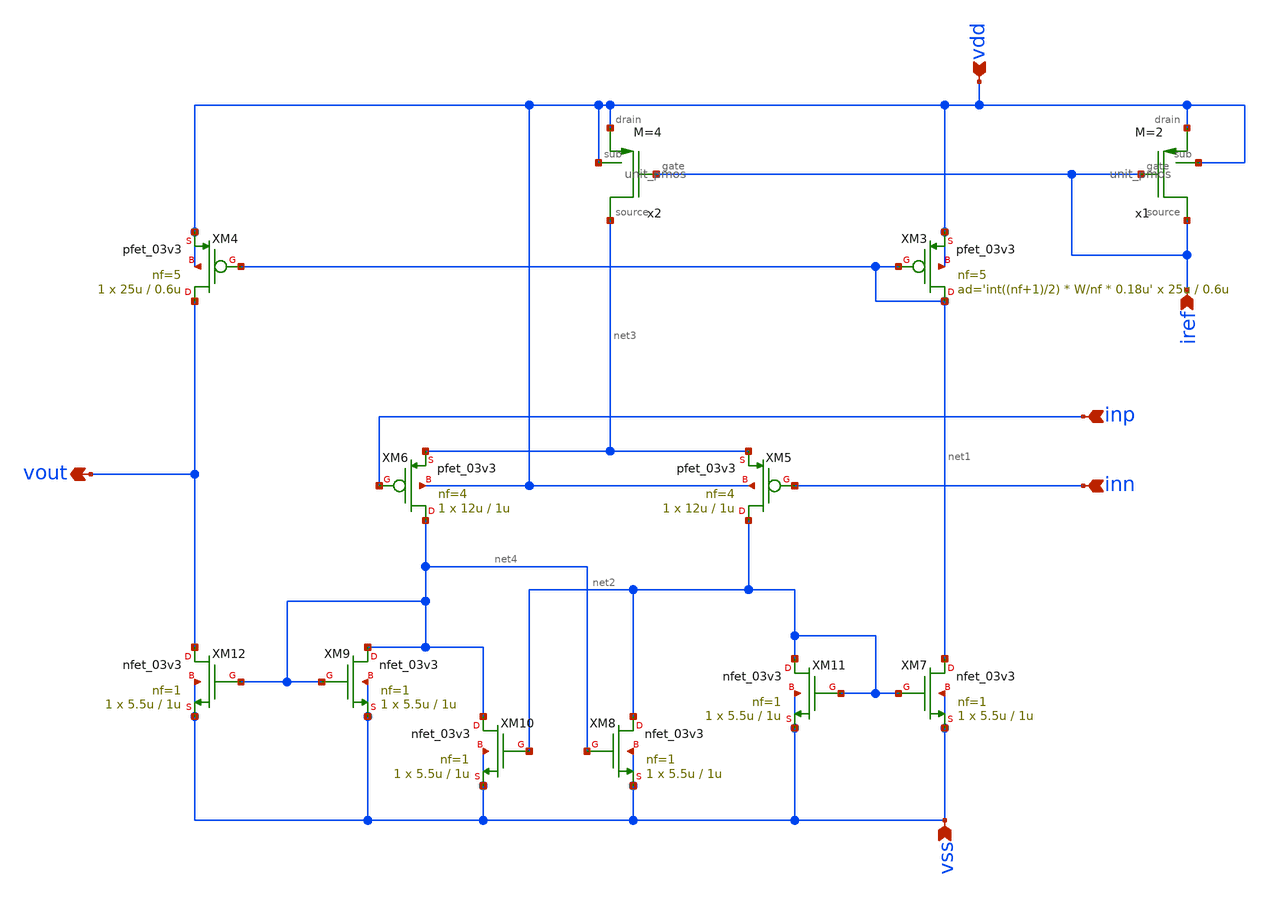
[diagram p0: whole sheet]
** sch_path: designs/libs/core_analog/Comparator/Pmos_Comparator.sch
**.subckt Pmos_Comparator vdd vss iref inn inp vout
*.ipin vdd
*.ipin vss
*.ipin iref
*.ipin inn
*.ipin inp
*.opin vout
XM3 net1 net1 vdd vdd pfet_03v3 L=0.6u W=25u nf=5 ad='int((nf+1)/2) * W/nf * 0.18u' as='int((nf+2)/2) * W/nf * 0.18u'
+ pd='2*int((nf+1)/2) * (W/nf + 0.18u)' ps='2*int((nf+2)/2) * (W/nf + 0.18u)' nrd='0.18u / W' nrs='0.18u / W'
+ sa=0 sb=0 sd=0 m=ad='int((nf+1)/2) * W/nf * 0.18u'
XM4 vout net1 vdd vdd pfet_03v3 L=0.6u W=25u nf=5 ad='int((nf+1)/2) * W/nf * 0.18u' as='int((nf+2)/2) * W/nf * 0.18u'
+ pd='2*int((nf+1)/2) * (W/nf + 0.18u)' ps='2*int((nf+2)/2) * (W/nf + 0.18u)' nrd='0.18u / W' nrs='0.18u / W'
+ sa=0 sb=0 sd=0 m=1
XM5 net2 inn net3 vdd pfet_03v3 L=1u W=12u nf=4 ad='int((nf+1)/2) * W/nf * 0.18u' as='int((nf+2)/2) * W/nf * 0.18u'
+ pd='2*int((nf+1)/2) * (W/nf + 0.18u)' ps='2*int((nf+2)/2) * (W/nf + 0.18u)' nrd='0.18u / W' nrs='0.18u / W'
+ sa=0 sb=0 sd=0 m=1
XM6 net4 inp net3 vdd pfet_03v3 L=1u W=12u nf=4 ad='int((nf+1)/2) * W/nf * 0.18u' as='int((nf+2)/2) * W/nf * 0.18u'
+ pd='2*int((nf+1)/2) * (W/nf + 0.18u)' ps='2*int((nf+2)/2) * (W/nf + 0.18u)' nrd='0.18u / W' nrs='0.18u / W'
+ sa=0 sb=0 sd=0 m=1
XM7 net1 net2 vss vss nfet_03v3 L=1u W=5.5u nf=1 ad='int((nf+1)/2) * W/nf * 0.18u' as='int((nf+2)/2) * W/nf * 0.18u'
+ pd='2*int((nf+1)/2) * (W/nf + 0.18u)' ps='2*int((nf+2)/2) * (W/nf + 0.18u)' nrd='0.18u / W' nrs='0.18u / W'
+ sa=0 sb=0 sd=0 m=1
XM8 net2 net4 vss vss nfet_03v3 L=1u W=5.5u nf=1 ad='int((nf+1)/2) * W/nf * 0.18u' as='int((nf+2)/2) * W/nf * 0.18u'
+ pd='2*int((nf+1)/2) * (W/nf + 0.18u)' ps='2*int((nf+2)/2) * (W/nf + 0.18u)' nrd='0.18u / W' nrs='0.18u / W'
+ sa=0 sb=0 sd=0 m=1
XM9 net4 net4 vss vss nfet_03v3 L=1u W=5.5u nf=1 ad='int((nf+1)/2) * W/nf * 0.18u' as='int((nf+2)/2) * W/nf * 0.18u'
+ pd='2*int((nf+1)/2) * (W/nf + 0.18u)' ps='2*int((nf+2)/2) * (W/nf + 0.18u)' nrd='0.18u / W' nrs='0.18u / W'
+ sa=0 sb=0 sd=0 m=1
XM10 net4 net2 vss vss nfet_03v3 L=1u W=5.5u nf=1 ad='int((nf+1)/2) * W/nf * 0.18u' as='int((nf+2)/2) * W/nf * 0.18u'
+ pd='2*int((nf+1)/2) * (W/nf + 0.18u)' ps='2*int((nf+2)/2) * (W/nf + 0.18u)' nrd='0.18u / W' nrs='0.18u / W'
+ sa=0 sb=0 sd=0 m=1
XM11 net2 net2 vss vss nfet_03v3 L=1u W=5.5u nf=1 ad='int((nf+1)/2) * W/nf * 0.18u' as='int((nf+2)/2) * W/nf * 0.18u'
+ pd='2*int((nf+1)/2) * (W/nf + 0.18u)' ps='2*int((nf+2)/2) * (W/nf + 0.18u)' nrd='0.18u / W' nrs='0.18u / W'
+ sa=0 sb=0 sd=0 m=1
XM12 vout net4 vss vss nfet_03v3 L=1u W=5.5u nf=1 ad='int((nf+1)/2) * W/nf * 0.18u' as='int((nf+2)/2) * W/nf * 0.18u'
+ pd='2*int((nf+1)/2) * (W/nf + 0.18u)' ps='2*int((nf+2)/2) * (W/nf + 0.18u)' nrd='0.18u / W' nrs='0.18u / W'
+ sa=0 sb=0 sd=0 m=1
x1 vdd vdd iref iref unit_pmos M=2
x2 vdd vdd iref net3 unit_pmos M=4
**.ends

* expanding   symbol:  libs/core_analog/unit_pmos/unit_pmos.sym # of pins=4
** sym_path: libs/core_analog/unit_pmos/unit_pmos.sym
** sch_path: libs/core_analog/unit_pmos/unit_pmos.sch
.subckt unit_pmos drain sub gate source
*.iopin drain
*.iopin source
*.iopin sub
*.iopin gate
**** begin user architecture code

.param M=1

**** end user architecture code
XM3 drain gate source sub pfet_03v3 L=1u W=3.5u nf=1 ad='int((nf+1)/2) * W/nf * 0.18u' as='int((nf+2)/2) * W/nf * 0.18u'
+ pd='2*int((nf+1)/2) * (W/nf + 0.18u)' ps='2*int((nf+2)/2) * (W/nf + 0.18u)' nrd='0.18u / W' nrs='0.18u / W'
+ sa=0 sb=0 sd=0 m={M}
.ends

.end
